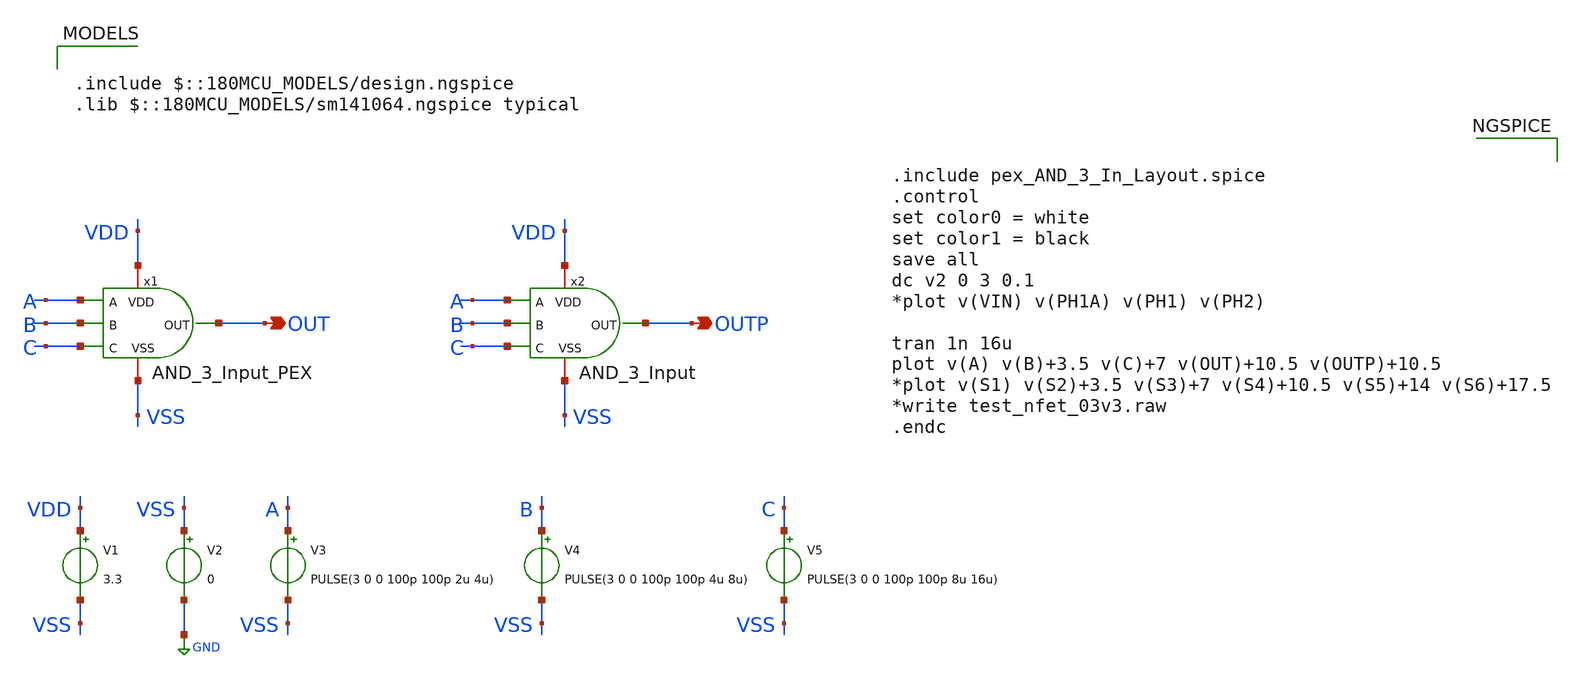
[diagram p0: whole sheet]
** sch_path: SCOP_INPUT_AND_MUX_PAKISTAN_03/Xschem/Logic_Gates/AND_3_Input_TB.sch
**.subckt AND_3_Input_TB OUT OUTP
*.opin OUT
*.opin OUTP
V1 VDD VSS 3.3
V2 VSS GND 0
V3 A VSS PULSE(3 0 0 100p 100p 2u 4u)
V4 B VSS PULSE(3 0 0 100p 100p 4u 8u)
V5 C VSS PULSE(3 0 0 100p 100p 8u 16u)
x1 VDD A OUT B C VSS AND_3_Input_PEX
x2 VDD A OUTP B C VSS AND_3_Input
**** begin user architecture code

.include $::180MCU_MODELS/design.ngspice
.lib $::180MCU_MODELS/sm141064.ngspice typical



.include pex_AND_3_In_Layout.spice
.control
set color0 = white
set color1 = black
save all
dc v2 0 3 0.1
*plot v(VIN) v(PH1A) v(PH1) v(PH2)

tran 1n 16u
plot v(A) v(B)+3.5 v(C)+7 v(OUT)+10.5 v(OUTP)+10.5
*plot v(S1) v(S2)+3.5 v(S3)+7 v(S4)+10.5 v(S5)+14 v(S6)+17.5
*write test_nfet_03v3.raw
.endc


**** end user architecture code
**.ends

* expanding   symbol:  AND_3_Input.sym # of pins=6
** sym_path: SCOP_INPUT_AND_MUX_PAKISTAN_03/Xschem/Logic_Gates/AND_3_Input.sym
** sch_path: SCOP_INPUT_AND_MUX_PAKISTAN_03/Xschem/Logic_Gates/AND_3_Input.sch
.subckt AND_3_Input VDD A OUT B C VSS
*.iopin VDD
*.iopin VSS
*.ipin A
*.ipin B
*.ipin C
*.opin OUT
XM1 net1 C VSS VSS nfet_03v3 L=0.28u W=1.5u nf=1 ad='int((nf+1)/2) * W/nf * 0.18u' as='int((nf+2)/2) * W/nf * 0.18u'
+ pd='2*int((nf+1)/2) * (W/nf + 0.18u)' ps='2*int((nf+2)/2) * (W/nf + 0.18u)' nrd='0.18u / W' nrs='0.18u / W'
+ sa=0 sb=0 sd=0 m=1
XM2 net3 A VDD VDD pfet_03v3 L=0.28u W=1u nf=1 ad='int((nf+1)/2) * W/nf * 0.18u' as='int((nf+2)/2) * W/nf * 0.18u'
+ pd='2*int((nf+1)/2) * (W/nf + 0.18u)' ps='2*int((nf+2)/2) * (W/nf + 0.18u)' nrd='0.18u / W' nrs='0.18u / W'
+ sa=0 sb=0 sd=0 m=1
XM3 net2 B net1 VSS nfet_03v3 L=0.28u W=1.5u nf=1 ad='int((nf+1)/2) * W/nf * 0.18u' as='int((nf+2)/2) * W/nf * 0.18u'
+ pd='2*int((nf+1)/2) * (W/nf + 0.18u)' ps='2*int((nf+2)/2) * (W/nf + 0.18u)' nrd='0.18u / W' nrs='0.18u / W'
+ sa=0 sb=0 sd=0 m=1
XM4 net3 A net2 VSS nfet_03v3 L=0.28u W=1.5u nf=1 ad='int((nf+1)/2) * W/nf * 0.18u' as='int((nf+2)/2) * W/nf * 0.18u'
+ pd='2*int((nf+1)/2) * (W/nf + 0.18u)' ps='2*int((nf+2)/2) * (W/nf + 0.18u)' nrd='0.18u / W' nrs='0.18u / W'
+ sa=0 sb=0 sd=0 m=1
XM5 net3 B VDD VDD pfet_03v3 L=0.28u W=1u nf=1 ad='int((nf+1)/2) * W/nf * 0.18u' as='int((nf+2)/2) * W/nf * 0.18u'
+ pd='2*int((nf+1)/2) * (W/nf + 0.18u)' ps='2*int((nf+2)/2) * (W/nf + 0.18u)' nrd='0.18u / W' nrs='0.18u / W'
+ sa=0 sb=0 sd=0 m=1
XM6 net3 C VDD VDD pfet_03v3 L=0.28u W=1u nf=1 ad='int((nf+1)/2) * W/nf * 0.18u' as='int((nf+2)/2) * W/nf * 0.18u'
+ pd='2*int((nf+1)/2) * (W/nf + 0.18u)' ps='2*int((nf+2)/2) * (W/nf + 0.18u)' nrd='0.18u / W' nrs='0.18u / W'
+ sa=0 sb=0 sd=0 m=1
XM8 OUT net3 VDD VDD pfet_03v3 L=0.28u W=1u nf=1 ad='int((nf+1)/2) * W/nf * 0.18u' as='int((nf+2)/2) * W/nf * 0.18u'
+ pd='2*int((nf+1)/2) * (W/nf + 0.18u)' ps='2*int((nf+2)/2) * (W/nf + 0.18u)' nrd='0.18u / W' nrs='0.18u / W'
+ sa=0 sb=0 sd=0 m=1
XM9 OUT net3 VSS VSS nfet_03v3 L=0.28u W=0.5u nf=1 ad='int((nf+1)/2) * W/nf * 0.18u' as='int((nf+2)/2) * W/nf * 0.18u'
+ pd='2*int((nf+1)/2) * (W/nf + 0.18u)' ps='2*int((nf+2)/2) * (W/nf + 0.18u)' nrd='0.18u / W' nrs='0.18u / W'
+ sa=0 sb=0 sd=0 m=1
.ends

.GLOBAL GND
.end
